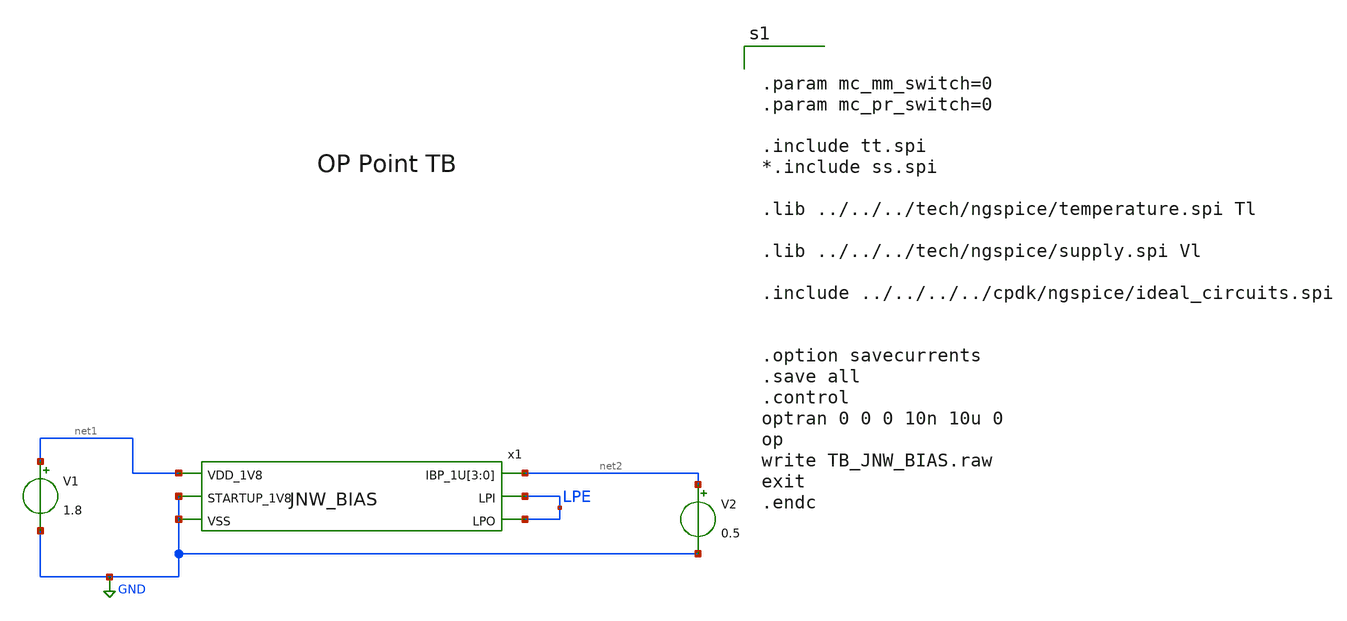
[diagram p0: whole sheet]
** sch_path: design/JNW_GR05_SKY130A/fuckRepo/TB_JNW_BIAS.sch
**.subckt TB_JNW_BIAS
x1 net1 LPE net2 net2 net2 net2 LPE GND GND JNW_BIAS
V1 net1 GND 1.8
V2 net2 GND 0.5
**** begin user architecture code


.param mc_mm_switch=0
.param mc_pr_switch=0

.include tt.spi
*.include ss.spi

.lib ../../../tech/ngspice/temperature.spi Tl

.lib ../../../tech/ngspice/supply.spi Vl

.include ../../../../cpdk/ngspice/ideal_circuits.spi


.option savecurrents
.save all
.control
optran 0 0 0 10n 10u 0
op
write TB_JNW_BIAS.raw
exit
.endc



**** end user architecture code
**.ends
.GLOBAL GND
.end
